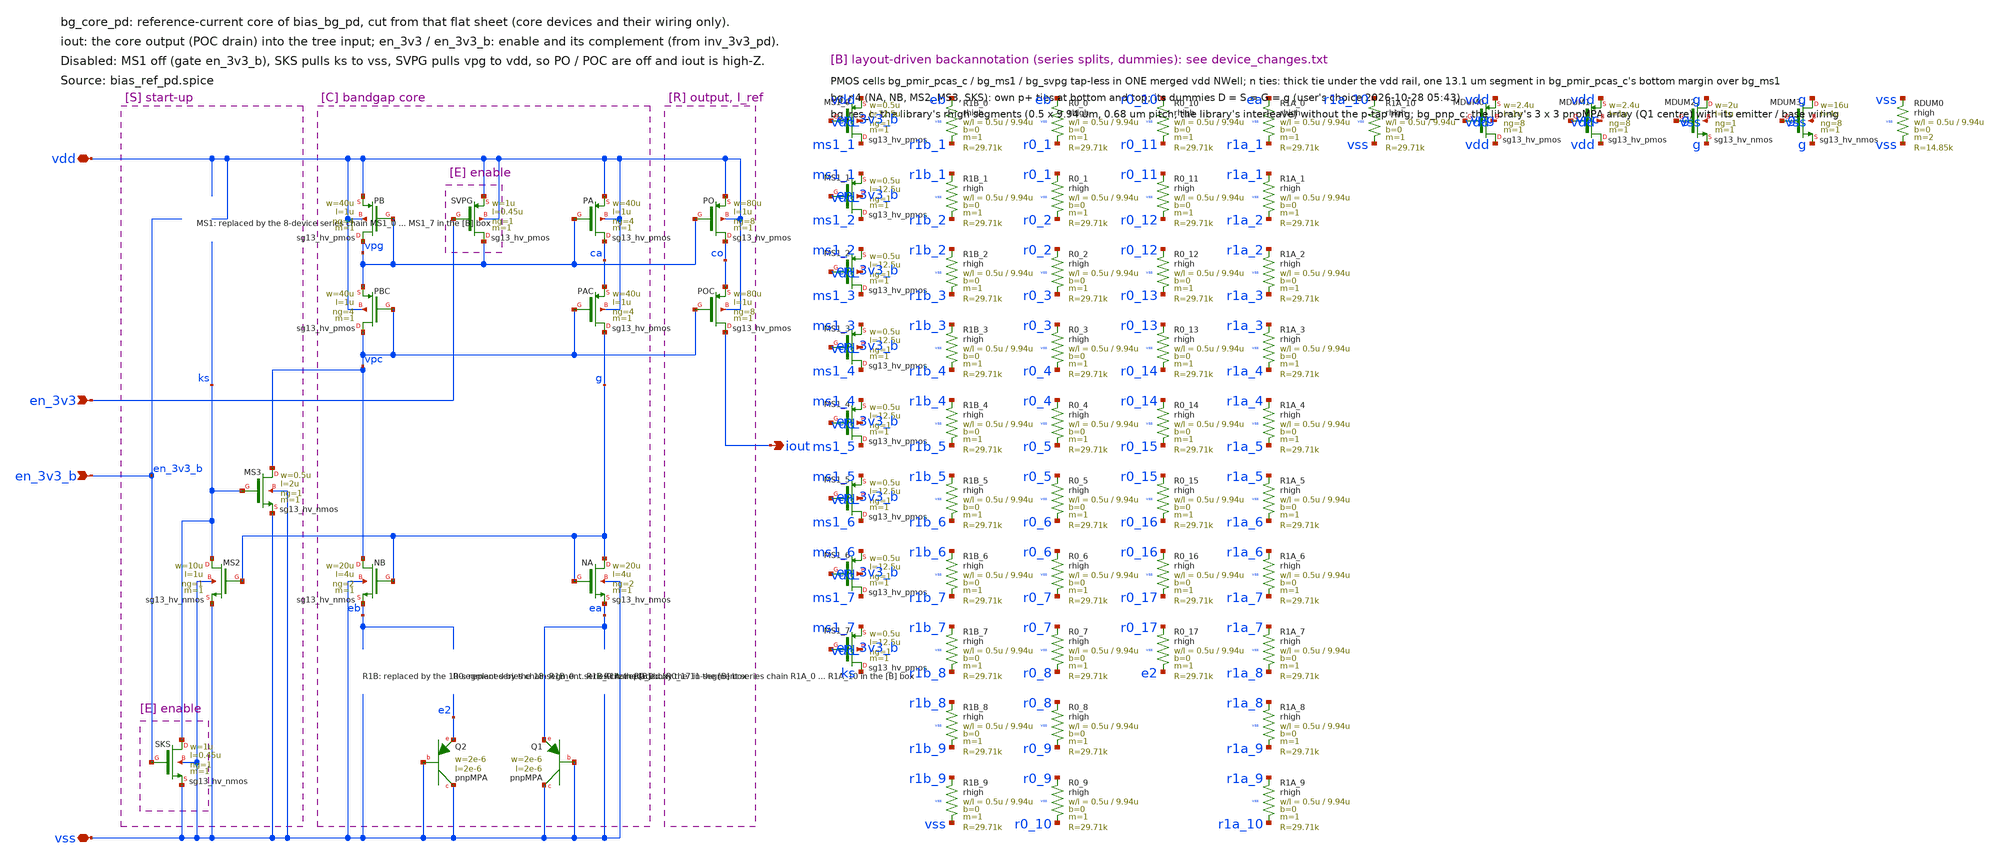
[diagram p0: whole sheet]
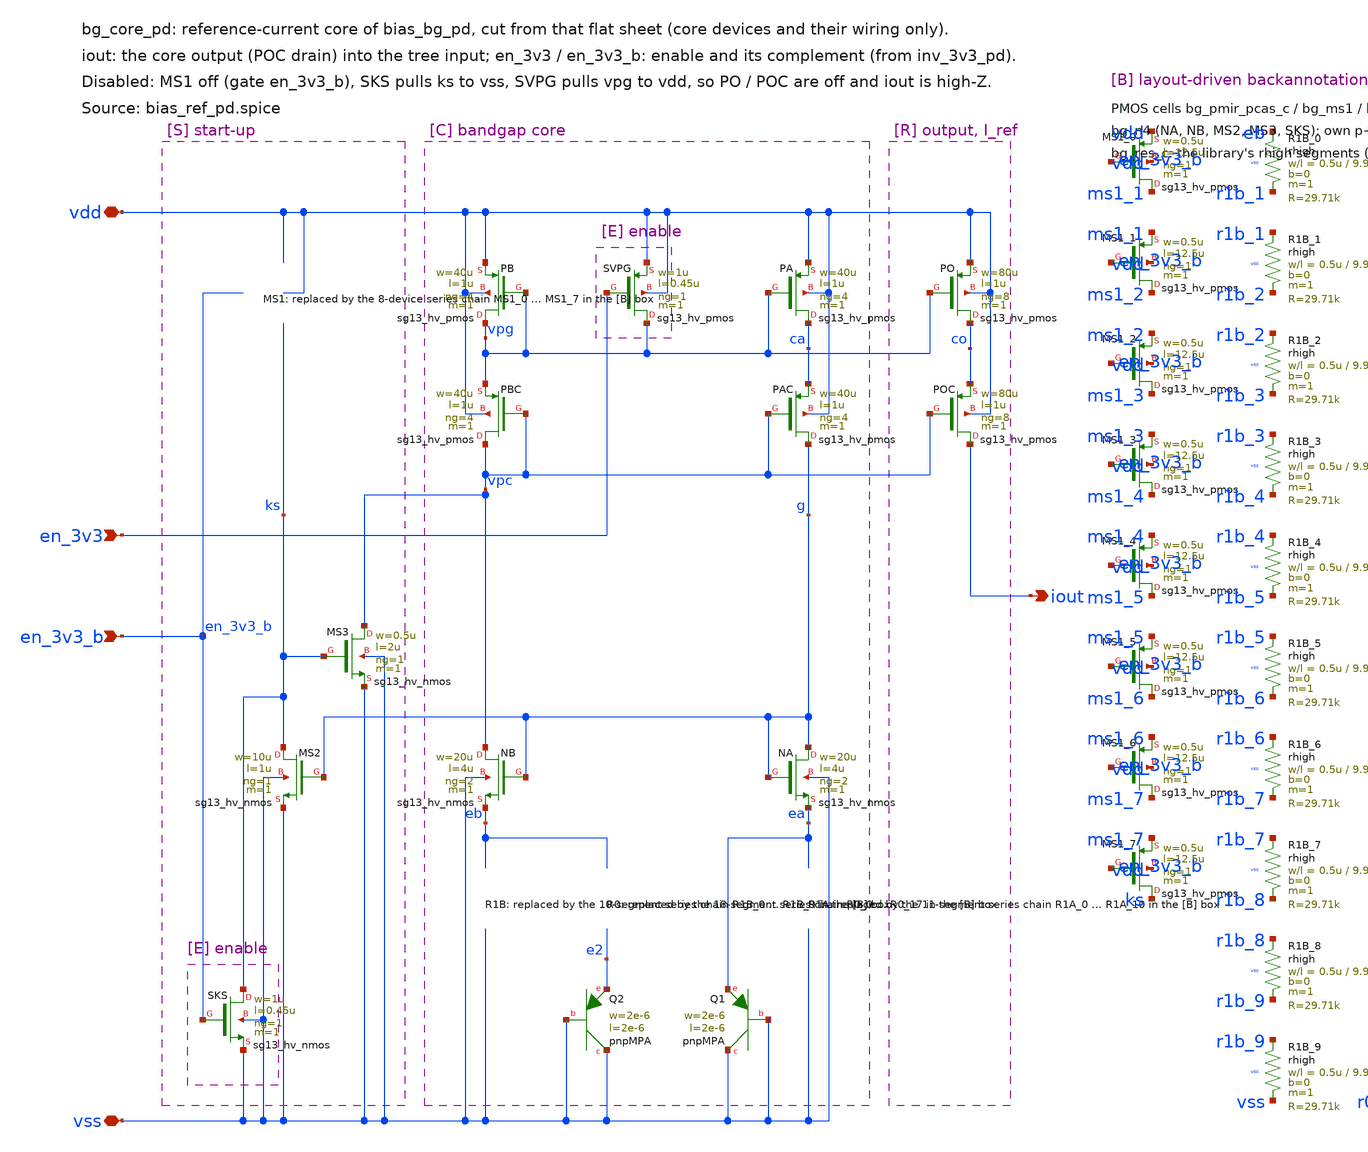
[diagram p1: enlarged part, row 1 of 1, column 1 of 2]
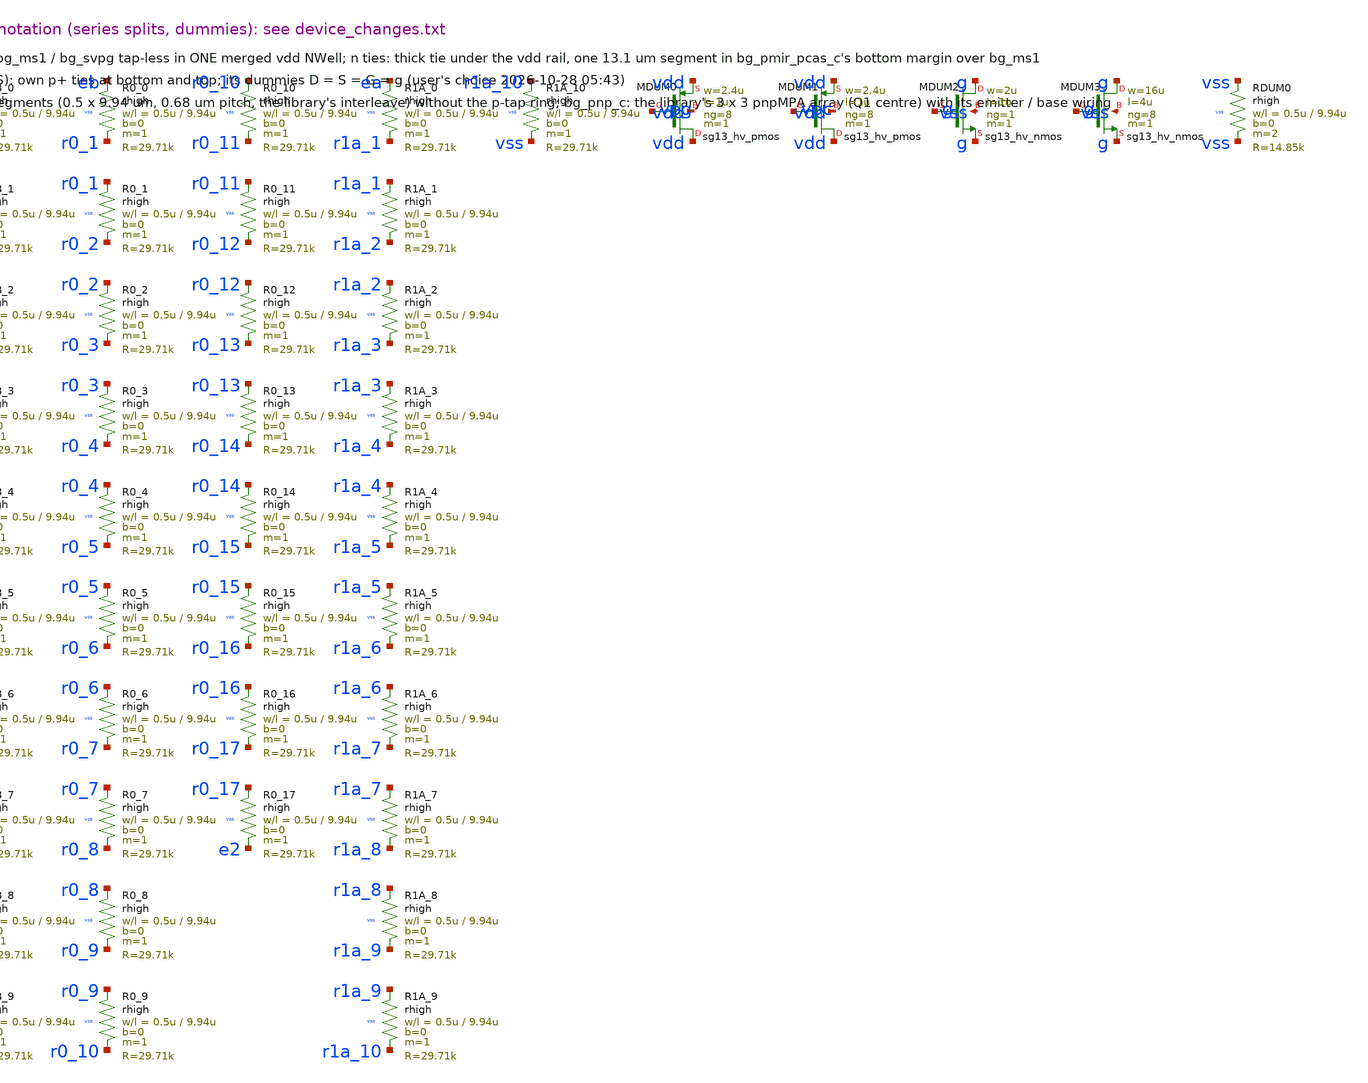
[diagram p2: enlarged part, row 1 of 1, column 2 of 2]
** sch_path: sudelbuecher/design_considerations/pad_buffer_layout/bg_core_pd_2026-10-28/backannotation/bg_core_pd.sch
**.subckt bg_core_pd vdd vss en_3v3 en_3v3_b iout
*.iopin vdd
*.iopin vss
*.ipin en_3v3
*.ipin en_3v3_b
*.opin iout
XMS2 ks g vss vss sg13_hv_nmos w=10u l=1u ng=1 m=1 mm_ok=1
XMS3 vpc ks vss vss sg13_hv_nmos w=0.5u l=2u ng=1 m=1 mm_ok=1
XPB vpg vpg vdd vdd sg13_hv_pmos w=40u l=1u ng=4 m=1 mm_ok=1
XPBC vpc vpc vpg vdd sg13_hv_pmos w=40u l=1u ng=4 m=1 mm_ok=1
XNB vpc g eb vss sg13_hv_nmos w=20u l=4u ng=2 m=1 mm_ok=1
XQ2 vss vss e2 pnpMPA a=4p p=8u m=8
XPA ca vpg vdd vdd sg13_hv_pmos w=40u l=1u ng=4 m=1 mm_ok=1
XPAC g vpc ca vdd sg13_hv_pmos w=40u l=1u ng=4 m=1 mm_ok=1
XNA g g ea vss sg13_hv_nmos w=20u l=4u ng=2 m=1 mm_ok=1
XQ1 vss vss ea pnpMPA a=4p p=8u m=1
XPO co vpg vdd vdd sg13_hv_pmos w=80u l=1u ng=8 m=1 mm_ok=1
XPOC iout vpc co vdd sg13_hv_pmos w=80u l=1u ng=8 m=1 mm_ok=1
XSKS ks en_3v3_b vss vss sg13_hv_nmos w=1u l=0.45u ng=1 m=1 mm_ok=1
XSVPG vpg en_3v3 vdd vdd sg13_hv_pmos w=1u l=0.45u ng=1 m=1 mm_ok=1
XMS1_0 ms1_1 en_3v3_b vdd vdd sg13_hv_pmos w=0.5u l=12.5u ng=1 m=1 mm_ok=1
XMS1_1 ms1_2 en_3v3_b ms1_1 vdd sg13_hv_pmos w=0.5u l=12.5u ng=1 m=1 mm_ok=1
XMS1_2 ms1_3 en_3v3_b ms1_2 vdd sg13_hv_pmos w=0.5u l=12.5u ng=1 m=1 mm_ok=1
XMS1_3 ms1_4 en_3v3_b ms1_3 vdd sg13_hv_pmos w=0.5u l=12.5u ng=1 m=1 mm_ok=1
XMS1_4 ms1_5 en_3v3_b ms1_4 vdd sg13_hv_pmos w=0.5u l=12.5u ng=1 m=1 mm_ok=1
XMS1_5 ms1_6 en_3v3_b ms1_5 vdd sg13_hv_pmos w=0.5u l=12.5u ng=1 m=1 mm_ok=1
XMS1_6 ms1_7 en_3v3_b ms1_6 vdd sg13_hv_pmos w=0.5u l=12.5u ng=1 m=1 mm_ok=1
XMS1_7 ks en_3v3_b ms1_7 vdd sg13_hv_pmos w=0.5u l=12.5u ng=1 m=1 mm_ok=1
XR1B_0 eb r1b_1 vss rhigh w=0.5u l=9.94u m=1 b=0 mm_ok=1
XR1B_1 r1b_1 r1b_2 vss rhigh w=0.5u l=9.94u m=1 b=0 mm_ok=1
XR1B_2 r1b_2 r1b_3 vss rhigh w=0.5u l=9.94u m=1 b=0 mm_ok=1
XR1B_3 r1b_3 r1b_4 vss rhigh w=0.5u l=9.94u m=1 b=0 mm_ok=1
XR1B_4 r1b_4 r1b_5 vss rhigh w=0.5u l=9.94u m=1 b=0 mm_ok=1
XR1B_5 r1b_5 r1b_6 vss rhigh w=0.5u l=9.94u m=1 b=0 mm_ok=1
XR1B_6 r1b_6 r1b_7 vss rhigh w=0.5u l=9.94u m=1 b=0 mm_ok=1
XR1B_7 r1b_7 r1b_8 vss rhigh w=0.5u l=9.94u m=1 b=0 mm_ok=1
XR1B_8 r1b_8 r1b_9 vss rhigh w=0.5u l=9.94u m=1 b=0 mm_ok=1
XR1B_9 r1b_9 vss vss rhigh w=0.5u l=9.94u m=1 b=0 mm_ok=1
XR0_0 eb r0_1 vss rhigh w=0.5u l=9.94u m=1 b=0 mm_ok=1
XR0_1 r0_1 r0_2 vss rhigh w=0.5u l=9.94u m=1 b=0 mm_ok=1
XR0_2 r0_2 r0_3 vss rhigh w=0.5u l=9.94u m=1 b=0 mm_ok=1
XR0_3 r0_3 r0_4 vss rhigh w=0.5u l=9.94u m=1 b=0 mm_ok=1
XR0_4 r0_4 r0_5 vss rhigh w=0.5u l=9.94u m=1 b=0 mm_ok=1
XR0_5 r0_5 r0_6 vss rhigh w=0.5u l=9.94u m=1 b=0 mm_ok=1
XR0_6 r0_6 r0_7 vss rhigh w=0.5u l=9.94u m=1 b=0 mm_ok=1
XR0_7 r0_7 r0_8 vss rhigh w=0.5u l=9.94u m=1 b=0 mm_ok=1
XR0_8 r0_8 r0_9 vss rhigh w=0.5u l=9.94u m=1 b=0 mm_ok=1
XR0_9 r0_9 r0_10 vss rhigh w=0.5u l=9.94u m=1 b=0 mm_ok=1
XR0_10 r0_10 r0_11 vss rhigh w=0.5u l=9.94u m=1 b=0 mm_ok=1
XR0_11 r0_11 r0_12 vss rhigh w=0.5u l=9.94u m=1 b=0 mm_ok=1
XR0_12 r0_12 r0_13 vss rhigh w=0.5u l=9.94u m=1 b=0 mm_ok=1
XR0_13 r0_13 r0_14 vss rhigh w=0.5u l=9.94u m=1 b=0 mm_ok=1
XR0_14 r0_14 r0_15 vss rhigh w=0.5u l=9.94u m=1 b=0 mm_ok=1
XR0_15 r0_15 r0_16 vss rhigh w=0.5u l=9.94u m=1 b=0 mm_ok=1
XR0_16 r0_16 r0_17 vss rhigh w=0.5u l=9.94u m=1 b=0 mm_ok=1
XR0_17 r0_17 e2 vss rhigh w=0.5u l=9.94u m=1 b=0 mm_ok=1
XR1A_0 ea r1a_1 vss rhigh w=0.5u l=9.94u m=1 b=0 mm_ok=1
XR1A_1 r1a_1 r1a_2 vss rhigh w=0.5u l=9.94u m=1 b=0 mm_ok=1
XR1A_2 r1a_2 r1a_3 vss rhigh w=0.5u l=9.94u m=1 b=0 mm_ok=1
XR1A_3 r1a_3 r1a_4 vss rhigh w=0.5u l=9.94u m=1 b=0 mm_ok=1
XR1A_4 r1a_4 r1a_5 vss rhigh w=0.5u l=9.94u m=1 b=0 mm_ok=1
XR1A_5 r1a_5 r1a_6 vss rhigh w=0.5u l=9.94u m=1 b=0 mm_ok=1
XR1A_6 r1a_6 r1a_7 vss rhigh w=0.5u l=9.94u m=1 b=0 mm_ok=1
XR1A_7 r1a_7 r1a_8 vss rhigh w=0.5u l=9.94u m=1 b=0 mm_ok=1
XR1A_8 r1a_8 r1a_9 vss rhigh w=0.5u l=9.94u m=1 b=0 mm_ok=1
XR1A_9 r1a_9 r1a_10 vss rhigh w=0.5u l=9.94u m=1 b=0 mm_ok=1
XR1A_10 r1a_10 vss vss rhigh w=0.5u l=9.94u m=1 b=0 mm_ok=1
XMDUM0 vdd vpg vdd vdd sg13_hv_pmos w=2.4u l=1u ng=8 m=1 mm_ok=1
XMDUM1 vdd vpc vdd vdd sg13_hv_pmos w=2.4u l=1u ng=8 m=1 mm_ok=1
XMDUM2 g g g vss sg13_hv_nmos w=2u l=1u ng=1 m=1 mm_ok=1
XMDUM3 g g g vss sg13_hv_nmos w=16u l=4u ng=8 m=1 mm_ok=1
XRDUM0 vss vss vss rhigh w=0.5u l=9.94u m=2 b=0 mm_ok=1
**.ends
.end
